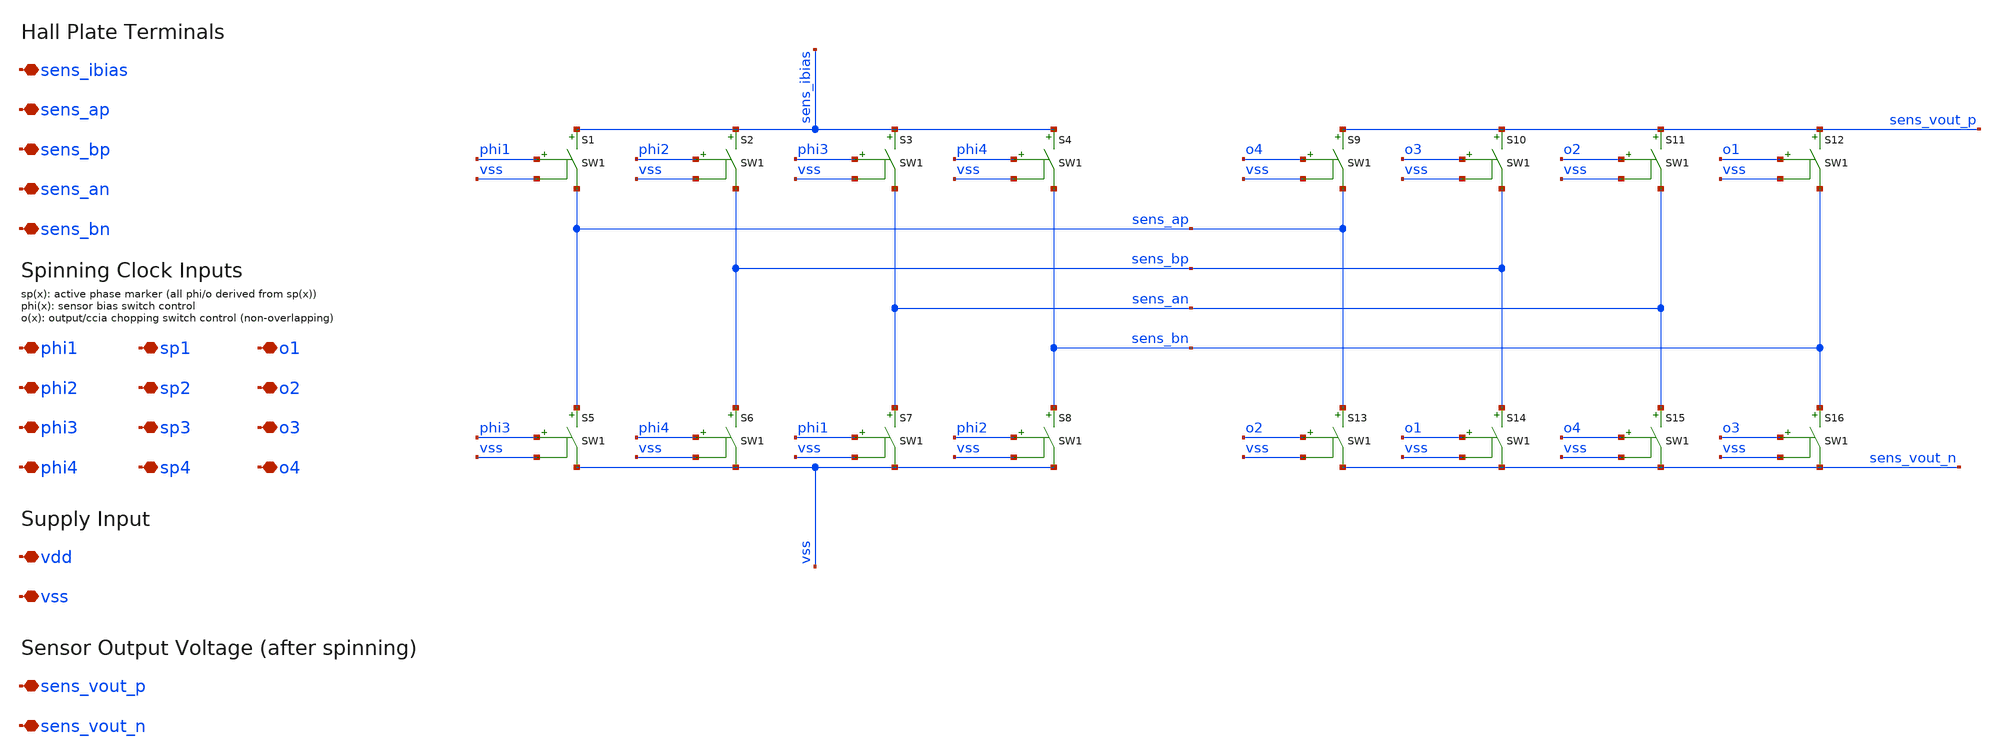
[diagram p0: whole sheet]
** sch_path: xschem/archive/spinning_current_gen_bhv/spinning_current_gen_bhv.sch
**.subckt spinning_current_gen_bhv sens_ap sens_bp sens_an sens_bn phi1 phi2 phi3 phi4 sp1 sp2 sp3
*+ sp4 o1 o2 o3 o4 sens_ibias sens_vout_p sens_vout_n vdd vss
*.iopin sens_ap
*.iopin sens_bp
*.iopin sens_an
*.iopin sens_bn
*.iopin phi1
*.iopin phi2
*.iopin phi3
*.iopin phi4
*.iopin sp1
*.iopin sp2
*.iopin sp3
*.iopin sp4
*.iopin o1
*.iopin o2
*.iopin o3
*.iopin o4
*.iopin sens_ibias
*.iopin sens_vout_p
*.iopin sens_vout_n
*.iopin vdd
*.iopin vss
S1 sens_ibias sens_ap phi1 vss SW1
S2 sens_ibias sens_bp phi2 vss SW1
S3 sens_ibias sens_an phi3 vss SW1
S4 sens_ibias sens_bn phi4 vss SW1
S5 sens_ap vss phi3 vss SW1
S6 sens_bp vss phi4 vss SW1
S7 sens_an vss phi1 vss SW1
S8 sens_bn vss phi2 vss SW1
S9 sens_vout_p sens_ap o4 vss SW1
S10 sens_vout_p sens_bp o3 vss SW1
S11 sens_vout_p sens_an o2 vss SW1
S12 sens_vout_p sens_bn o1 vss SW1
S13 sens_ap sens_vout_n o2 vss SW1
S14 sens_bp sens_vout_n o1 vss SW1
S15 sens_an sens_vout_n o4 vss SW1
S16 sens_bn sens_vout_n o3 vss SW1
**.ends
**** begin user architecture code
.MODEL SW1 SW   VT=1.65 VH=0.01  RON=100 ROFF=1G
**** end user architecture code
.end
